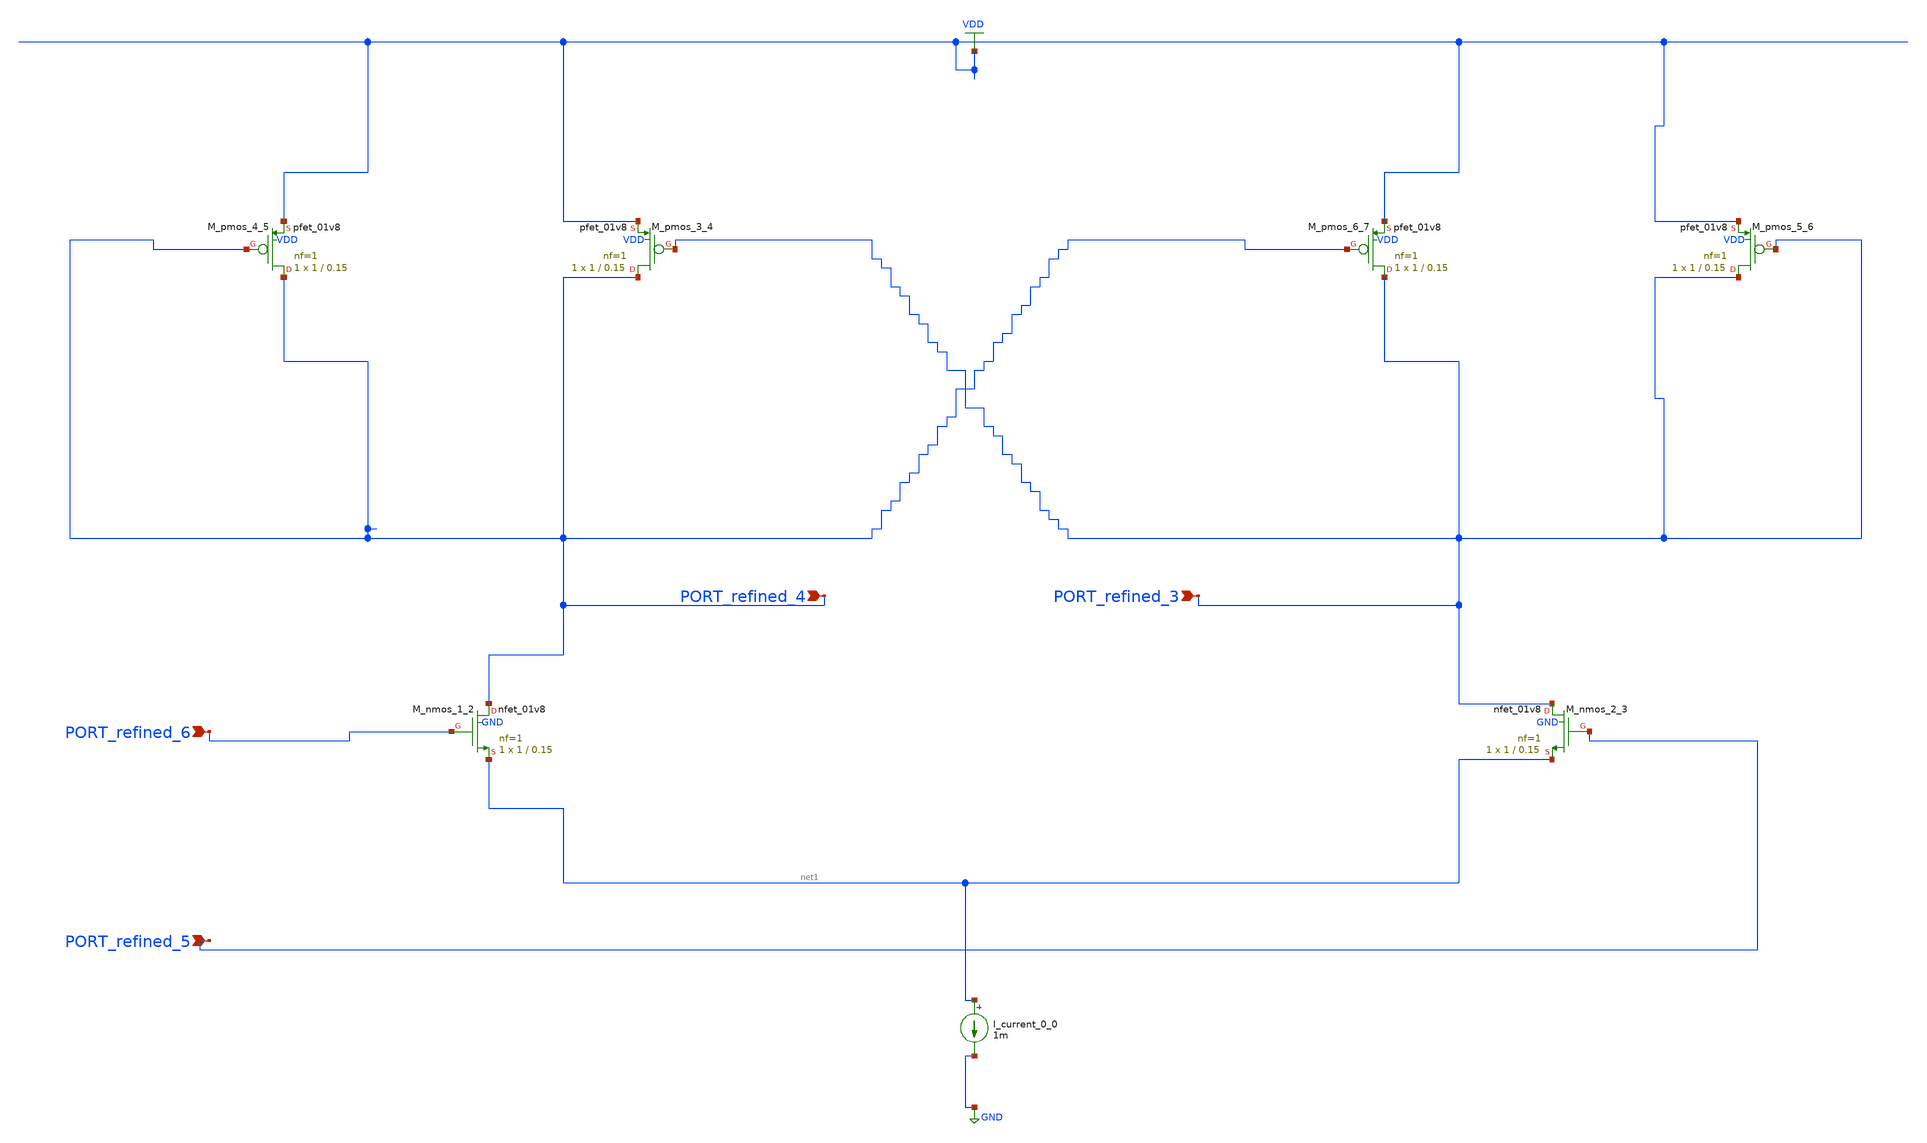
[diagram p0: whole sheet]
** sch_path: schematics/AMSNet/525.sch
**.subckt 525 PORT_refined_4 PORT_refined_5 PORT_refined_3 PORT_refined_6
*.ipin PORT_refined_4
*.ipin PORT_refined_5
*.ipin PORT_refined_3
*.ipin PORT_refined_6
I_current_0_0 net1 GND 1m
XM_nmos_1_2 PORT_refined_4 PORT_refined_6 net1 GND sky130_fd_pr__nfet_01v8 L=0.15 W=1 nf=1 ad='int((1 + 1)/2) * 1 / 1 * 0.29'
+ as='int((1 + 2)/2) * 1 / 1 * 0.29' pd='2*int((1 + 1)/2) * (1 / 1 + 0.29)' ps='2*int((1 + 2)/2) * (1 / 1 + 0.29)'
+ nrd='0.29 / 1 ' nrs='0.29 / 1 ' sa=0 sb=0 sd=0 mult=1 m=1
XM_nmos_2_3 PORT_refined_3 PORT_refined_5 net1 GND sky130_fd_pr__nfet_01v8 L=0.15 W=1 nf=1 ad='int((1 + 1)/2) * 1 / 1 * 0.29'
+ as='int((1 + 2)/2) * 1 / 1 * 0.29' pd='2*int((1 + 1)/2) * (1 / 1 + 0.29)' ps='2*int((1 + 2)/2) * (1 / 1 + 0.29)'
+ nrd='0.29 / 1 ' nrs='0.29 / 1 ' sa=0 sb=0 sd=0 mult=1 m=1
XM_pmos_3_4 PORT_refined_4 PORT_refined_3 VDD VDD sky130_fd_pr__pfet_01v8 L=0.15 W=1 nf=1 ad='int((1 + 1)/2) * 1 / 1 * 0.29'
+ as='int((1 + 2)/2) * 1 / 1 * 0.29' pd='2*int((1 + 1)/2) * (1 / 1 + 0.29)' ps='2*int((1 + 2)/2) * (1 / 1 + 0.29)'
+ nrd='0.29 / 1 ' nrs='0.29 / 1 ' sa=0 sb=0 sd=0 mult=1 m=1
XM_pmos_4_5 PORT_refined_4 PORT_refined_4 VDD VDD sky130_fd_pr__pfet_01v8 L=0.15 W=1 nf=1 ad='int((1 + 1)/2) * 1 / 1 * 0.29'
+ as='int((1 + 2)/2) * 1 / 1 * 0.29' pd='2*int((1 + 1)/2) * (1 / 1 + 0.29)' ps='2*int((1 + 2)/2) * (1 / 1 + 0.29)'
+ nrd='0.29 / 1 ' nrs='0.29 / 1 ' sa=0 sb=0 sd=0 mult=1 m=1
XM_pmos_5_6 PORT_refined_3 PORT_refined_3 VDD VDD sky130_fd_pr__pfet_01v8 L=0.15 W=1 nf=1 ad='int((1 + 1)/2) * 1 / 1 * 0.29'
+ as='int((1 + 2)/2) * 1 / 1 * 0.29' pd='2*int((1 + 1)/2) * (1 / 1 + 0.29)' ps='2*int((1 + 2)/2) * (1 / 1 + 0.29)'
+ nrd='0.29 / 1 ' nrs='0.29 / 1 ' sa=0 sb=0 sd=0 mult=1 m=1
XM_pmos_6_7 PORT_refined_3 PORT_refined_4 VDD VDD sky130_fd_pr__pfet_01v8 L=0.15 W=1 nf=1 ad='int((1 + 1)/2) * 1 / 1 * 0.29'
+ as='int((1 + 2)/2) * 1 / 1 * 0.29' pd='2*int((1 + 1)/2) * (1 / 1 + 0.29)' ps='2*int((1 + 2)/2) * (1 / 1 + 0.29)'
+ nrd='0.29 / 1 ' nrs='0.29 / 1 ' sa=0 sb=0 sd=0 mult=1 m=1
**.ends
.GLOBAL GND
.GLOBAL VDD
.end
